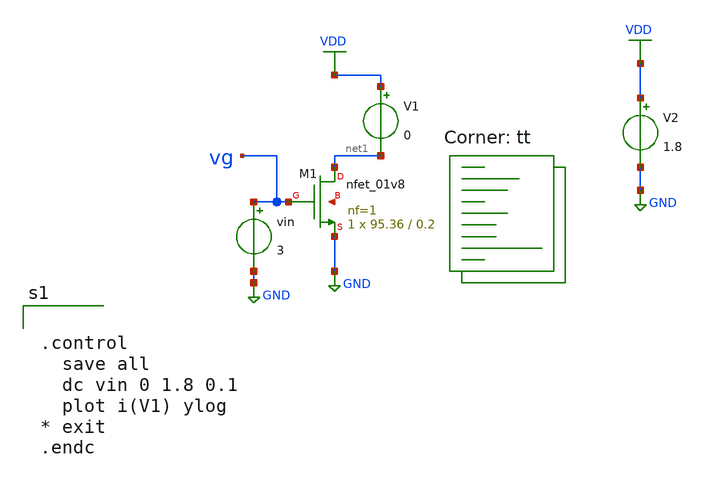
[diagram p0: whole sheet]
** sch_path: project2/test_schem.sch
**.subckt test_schem
vin vg GND 3
V2 VDD GND 1.8
V1 VDD net1 0
XM1 net1 vg GND net2 sky130_fd_pr__nfet_01v8 L=0.2 W=95.36 nf=1 ad='int((nf+1)/2) * W/nf * 0.29' as='int((nf+2)/2) * W/nf * 0.29'
+ pd='2*int((nf+1)/2) * (W/nf + 0.29)' ps='2*int((nf+2)/2) * (W/nf + 0.29)' nrd='0.29 / W' nrs='0.29 / W'
+ sa=0 sb=0 sd=0 mult=1 m=1
**** begin user architecture code
.lib $::SKYWATER_MODELS/sky130.lib.spice tt


.control
  save all
  dc vin 0 1.8 0.1
  plot i(V1) ylog
* exit
.endc


**** end user architecture code
**.ends
.GLOBAL GND
.GLOBAL VDD
.end
